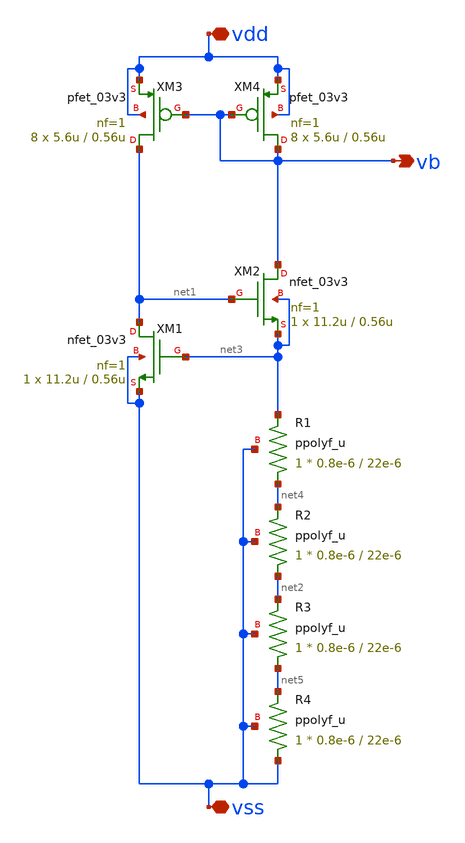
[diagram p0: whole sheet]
** sch_path: 1st_Design/cs-vth-ref.sch
**.subckt cs-vth-ref vdd vss vb
*.iopin vdd
*.iopin vss
*.opin vb
XM1 net1 net3 vss vss nfet_03v3 L=0.56u W=11.2u nf=1 ad='int((nf+1)/2) * W/nf * 0.18u' as='int((nf+2)/2) * W/nf * 0.18u'
+ pd='2*int((nf+1)/2) * (W/nf + 0.18u)' ps='2*int((nf+2)/2) * (W/nf + 0.18u)' nrd='0.18u / W' nrs='0.18u / W'
+ sa=0 sb=0 sd=0 m=1
XM2 vb net1 net3 net3 nfet_03v3 L=0.56u W=11.2u nf=1 ad='int((nf+1)/2) * W/nf * 0.18u' as='int((nf+2)/2) * W/nf * 0.18u'
+ pd='2*int((nf+1)/2) * (W/nf + 0.18u)' ps='2*int((nf+2)/2) * (W/nf + 0.18u)' nrd='0.18u / W' nrs='0.18u / W'
+ sa=0 sb=0 sd=0 m=1
XM3 net1 vb vdd vdd pfet_03v3 L=0.56u W=5.6u nf=1 ad='int((nf+1)/2) * W/nf * 0.18u' as='int((nf+2)/2) * W/nf * 0.18u'
+ pd='2*int((nf+1)/2) * (W/nf + 0.18u)' ps='2*int((nf+2)/2) * (W/nf + 0.18u)' nrd='0.18u / W' nrs='0.18u / W'
+ sa=0 sb=0 sd=0 m=8
XM4 vb vb vdd vdd pfet_03v3 L=0.56u W=5.6u nf=1 ad='int((nf+1)/2) * W/nf * 0.18u' as='int((nf+2)/2) * W/nf * 0.18u'
+ pd='2*int((nf+1)/2) * (W/nf + 0.18u)' ps='2*int((nf+2)/2) * (W/nf + 0.18u)' nrd='0.18u / W' nrs='0.18u / W'
+ sa=0 sb=0 sd=0 m=8
XR2 net2 net4 vss ppolyf_u r_width=0.8e-6 r_length=22e-6 m=1
XR1 net4 net3 vss ppolyf_u r_width=0.8e-6 r_length=22e-6 m=1
XR3 net5 net2 vss ppolyf_u r_width=0.8e-6 r_length=22e-6 m=1
XR4 vss net5 vss ppolyf_u r_width=0.8e-6 r_length=22e-6 m=1
**.ends
.end
